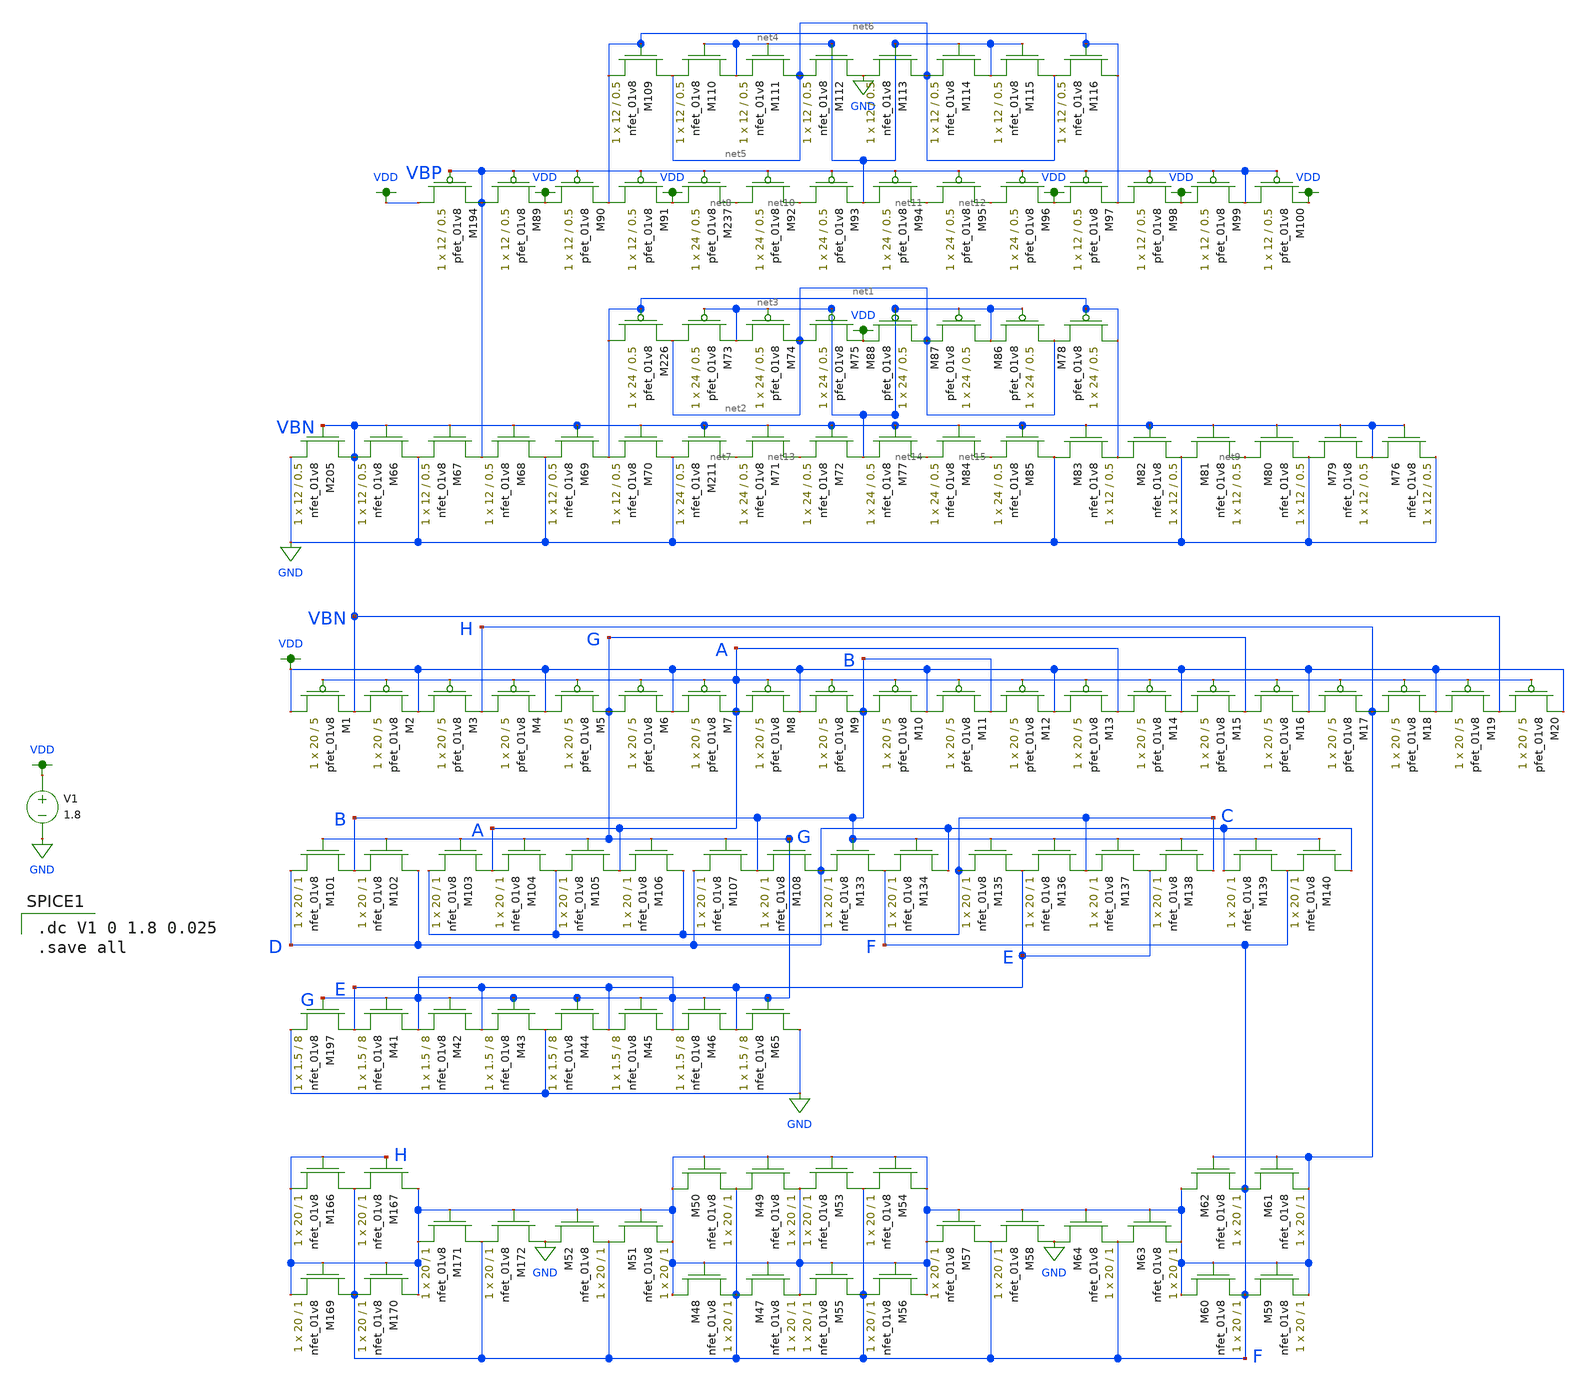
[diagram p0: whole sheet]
** sch_path: miniproject_03/xschem/bias_gen_layout_gen4.sch
**.subckt bias_gen_layout_gen4
XM1 VDD A VBN VDD sky130_fd_pr__pfet_01v8 L=5 W=20 nf=1 ad='int((nf+1)/2) * W/nf * 0.29' as='int((nf+2)/2) * W/nf * 0.29'
+ pd='2*int((nf+1)/2) * (W/nf + 0.29)' ps='2*int((nf+2)/2) * (W/nf + 0.29)' nrd='0.29 / W' nrs='0.29 / W'
+ sa=0 sb=0 sd=0 mult=1 m=1
XM2 VBN A VDD VDD sky130_fd_pr__pfet_01v8 L=5 W=20 nf=1 ad='int((nf+1)/2) * W/nf * 0.29' as='int((nf+2)/2) * W/nf * 0.29'
+ pd='2*int((nf+1)/2) * (W/nf + 0.29)' ps='2*int((nf+2)/2) * (W/nf + 0.29)' nrd='0.29 / W' nrs='0.29 / W'
+ sa=0 sb=0 sd=0 mult=1 m=1
XM3 VDD A H VDD sky130_fd_pr__pfet_01v8 L=5 W=20 nf=1 ad='int((nf+1)/2) * W/nf * 0.29' as='int((nf+2)/2) * W/nf * 0.29'
+ pd='2*int((nf+1)/2) * (W/nf + 0.29)' ps='2*int((nf+2)/2) * (W/nf + 0.29)' nrd='0.29 / W' nrs='0.29 / W'
+ sa=0 sb=0 sd=0 mult=1 m=1
XM4 H A VDD VDD sky130_fd_pr__pfet_01v8 L=5 W=20 nf=1 ad='int((nf+1)/2) * W/nf * 0.29' as='int((nf+2)/2) * W/nf * 0.29'
+ pd='2*int((nf+1)/2) * (W/nf + 0.29)' ps='2*int((nf+2)/2) * (W/nf + 0.29)' nrd='0.29 / W' nrs='0.29 / W'
+ sa=0 sb=0 sd=0 mult=1 m=1
XM5 VDD A G VDD sky130_fd_pr__pfet_01v8 L=5 W=20 nf=1 ad='int((nf+1)/2) * W/nf * 0.29' as='int((nf+2)/2) * W/nf * 0.29'
+ pd='2*int((nf+1)/2) * (W/nf + 0.29)' ps='2*int((nf+2)/2) * (W/nf + 0.29)' nrd='0.29 / W' nrs='0.29 / W'
+ sa=0 sb=0 sd=0 mult=1 m=1
XM6 G A VDD VDD sky130_fd_pr__pfet_01v8 L=5 W=20 nf=1 ad='int((nf+1)/2) * W/nf * 0.29' as='int((nf+2)/2) * W/nf * 0.29'
+ pd='2*int((nf+1)/2) * (W/nf + 0.29)' ps='2*int((nf+2)/2) * (W/nf + 0.29)' nrd='0.29 / W' nrs='0.29 / W'
+ sa=0 sb=0 sd=0 mult=1 m=1
XM7 VDD A A VDD sky130_fd_pr__pfet_01v8 L=5 W=20 nf=1 ad='int((nf+1)/2) * W/nf * 0.29' as='int((nf+2)/2) * W/nf * 0.29'
+ pd='2*int((nf+1)/2) * (W/nf + 0.29)' ps='2*int((nf+2)/2) * (W/nf + 0.29)' nrd='0.29 / W' nrs='0.29 / W'
+ sa=0 sb=0 sd=0 mult=1 m=1
XM8 A A VDD VDD sky130_fd_pr__pfet_01v8 L=5 W=20 nf=1 ad='int((nf+1)/2) * W/nf * 0.29' as='int((nf+2)/2) * W/nf * 0.29'
+ pd='2*int((nf+1)/2) * (W/nf + 0.29)' ps='2*int((nf+2)/2) * (W/nf + 0.29)' nrd='0.29 / W' nrs='0.29 / W'
+ sa=0 sb=0 sd=0 mult=1 m=1
XM9 VDD A B VDD sky130_fd_pr__pfet_01v8 L=5 W=20 nf=1 ad='int((nf+1)/2) * W/nf * 0.29' as='int((nf+2)/2) * W/nf * 0.29'
+ pd='2*int((nf+1)/2) * (W/nf + 0.29)' ps='2*int((nf+2)/2) * (W/nf + 0.29)' nrd='0.29 / W' nrs='0.29 / W'
+ sa=0 sb=0 sd=0 mult=1 m=1
XM10 B A VDD VDD sky130_fd_pr__pfet_01v8 L=5 W=20 nf=1 ad='int((nf+1)/2) * W/nf * 0.29' as='int((nf+2)/2) * W/nf * 0.29'
+ pd='2*int((nf+1)/2) * (W/nf + 0.29)' ps='2*int((nf+2)/2) * (W/nf + 0.29)' nrd='0.29 / W' nrs='0.29 / W'
+ sa=0 sb=0 sd=0 mult=1 m=1
XM11 VDD A B VDD sky130_fd_pr__pfet_01v8 L=5 W=20 nf=1 ad='int((nf+1)/2) * W/nf * 0.29' as='int((nf+2)/2) * W/nf * 0.29'
+ pd='2*int((nf+1)/2) * (W/nf + 0.29)' ps='2*int((nf+2)/2) * (W/nf + 0.29)' nrd='0.29 / W' nrs='0.29 / W'
+ sa=0 sb=0 sd=0 mult=1 m=1
XM12 B A VDD VDD sky130_fd_pr__pfet_01v8 L=5 W=20 nf=1 ad='int((nf+1)/2) * W/nf * 0.29' as='int((nf+2)/2) * W/nf * 0.29'
+ pd='2*int((nf+1)/2) * (W/nf + 0.29)' ps='2*int((nf+2)/2) * (W/nf + 0.29)' nrd='0.29 / W' nrs='0.29 / W'
+ sa=0 sb=0 sd=0 mult=1 m=1
XM13 VDD A A VDD sky130_fd_pr__pfet_01v8 L=5 W=20 nf=1 ad='int((nf+1)/2) * W/nf * 0.29' as='int((nf+2)/2) * W/nf * 0.29'
+ pd='2*int((nf+1)/2) * (W/nf + 0.29)' ps='2*int((nf+2)/2) * (W/nf + 0.29)' nrd='0.29 / W' nrs='0.29 / W'
+ sa=0 sb=0 sd=0 mult=1 m=1
XM14 A A VDD VDD sky130_fd_pr__pfet_01v8 L=5 W=20 nf=1 ad='int((nf+1)/2) * W/nf * 0.29' as='int((nf+2)/2) * W/nf * 0.29'
+ pd='2*int((nf+1)/2) * (W/nf + 0.29)' ps='2*int((nf+2)/2) * (W/nf + 0.29)' nrd='0.29 / W' nrs='0.29 / W'
+ sa=0 sb=0 sd=0 mult=1 m=1
XM15 VDD A G VDD sky130_fd_pr__pfet_01v8 L=5 W=20 nf=1 ad='int((nf+1)/2) * W/nf * 0.29' as='int((nf+2)/2) * W/nf * 0.29'
+ pd='2*int((nf+1)/2) * (W/nf + 0.29)' ps='2*int((nf+2)/2) * (W/nf + 0.29)' nrd='0.29 / W' nrs='0.29 / W'
+ sa=0 sb=0 sd=0 mult=1 m=1
XM16 G A VDD VDD sky130_fd_pr__pfet_01v8 L=5 W=20 nf=1 ad='int((nf+1)/2) * W/nf * 0.29' as='int((nf+2)/2) * W/nf * 0.29'
+ pd='2*int((nf+1)/2) * (W/nf + 0.29)' ps='2*int((nf+2)/2) * (W/nf + 0.29)' nrd='0.29 / W' nrs='0.29 / W'
+ sa=0 sb=0 sd=0 mult=1 m=1
XM17 VDD A H VDD sky130_fd_pr__pfet_01v8 L=5 W=20 nf=1 ad='int((nf+1)/2) * W/nf * 0.29' as='int((nf+2)/2) * W/nf * 0.29'
+ pd='2*int((nf+1)/2) * (W/nf + 0.29)' ps='2*int((nf+2)/2) * (W/nf + 0.29)' nrd='0.29 / W' nrs='0.29 / W'
+ sa=0 sb=0 sd=0 mult=1 m=1
XM18 H A VDD VDD sky130_fd_pr__pfet_01v8 L=5 W=20 nf=1 ad='int((nf+1)/2) * W/nf * 0.29' as='int((nf+2)/2) * W/nf * 0.29'
+ pd='2*int((nf+1)/2) * (W/nf + 0.29)' ps='2*int((nf+2)/2) * (W/nf + 0.29)' nrd='0.29 / W' nrs='0.29 / W'
+ sa=0 sb=0 sd=0 mult=1 m=1
XM19 VDD A VBN VDD sky130_fd_pr__pfet_01v8 L=5 W=20 nf=1 ad='int((nf+1)/2) * W/nf * 0.29' as='int((nf+2)/2) * W/nf * 0.29'
+ pd='2*int((nf+1)/2) * (W/nf + 0.29)' ps='2*int((nf+2)/2) * (W/nf + 0.29)' nrd='0.29 / W' nrs='0.29 / W'
+ sa=0 sb=0 sd=0 mult=1 m=1
XM20 VBN A VDD VDD sky130_fd_pr__pfet_01v8 L=5 W=20 nf=1 ad='int((nf+1)/2) * W/nf * 0.29' as='int((nf+2)/2) * W/nf * 0.29'
+ pd='2*int((nf+1)/2) * (W/nf + 0.29)' ps='2*int((nf+2)/2) * (W/nf + 0.29)' nrd='0.29 / W' nrs='0.29 / W'
+ sa=0 sb=0 sd=0 mult=1 m=1
XM166 F H H GND sky130_fd_pr__nfet_01v8 L=1 W=20 nf=1 ad='int((nf+1)/2) * W/nf * 0.29' as='int((nf+2)/2) * W/nf * 0.29'
+ pd='2*int((nf+1)/2) * (W/nf + 0.29)' ps='2*int((nf+2)/2) * (W/nf + 0.29)' nrd='0.29 / W' nrs='0.29 / W'
+ sa=0 sb=0 sd=0 mult=1 m=1
XM167 H H F GND sky130_fd_pr__nfet_01v8 L=1 W=20 nf=1 ad='int((nf+1)/2) * W/nf * 0.29' as='int((nf+2)/2) * W/nf * 0.29'
+ pd='2*int((nf+1)/2) * (W/nf + 0.29)' ps='2*int((nf+2)/2) * (W/nf + 0.29)' nrd='0.29 / W' nrs='0.29 / W'
+ sa=0 sb=0 sd=0 mult=1 m=1
XM169 F H H GND sky130_fd_pr__nfet_01v8 L=1 W=20 nf=1 ad='int((nf+1)/2) * W/nf * 0.29' as='int((nf+2)/2) * W/nf * 0.29'
+ pd='2*int((nf+1)/2) * (W/nf + 0.29)' ps='2*int((nf+2)/2) * (W/nf + 0.29)' nrd='0.29 / W' nrs='0.29 / W'
+ sa=0 sb=0 sd=0 mult=1 m=1
XM170 H H F GND sky130_fd_pr__nfet_01v8 L=1 W=20 nf=1 ad='int((nf+1)/2) * W/nf * 0.29' as='int((nf+2)/2) * W/nf * 0.29'
+ pd='2*int((nf+1)/2) * (W/nf + 0.29)' ps='2*int((nf+2)/2) * (W/nf + 0.29)' nrd='0.29 / W' nrs='0.29 / W'
+ sa=0 sb=0 sd=0 mult=1 m=1
XM171 F H H GND sky130_fd_pr__nfet_01v8 L=1 W=20 nf=1 ad='int((nf+1)/2) * W/nf * 0.29' as='int((nf+2)/2) * W/nf * 0.29'
+ pd='2*int((nf+1)/2) * (W/nf + 0.29)' ps='2*int((nf+2)/2) * (W/nf + 0.29)' nrd='0.29 / W' nrs='0.29 / W'
+ sa=0 sb=0 sd=0 mult=1 m=1
XM172 GND H F GND sky130_fd_pr__nfet_01v8 L=1 W=20 nf=1 ad='int((nf+1)/2) * W/nf * 0.29' as='int((nf+2)/2) * W/nf * 0.29'
+ pd='2*int((nf+1)/2) * (W/nf + 0.29)' ps='2*int((nf+2)/2) * (W/nf + 0.29)' nrd='0.29 / W' nrs='0.29 / W'
+ sa=0 sb=0 sd=0 mult=1 m=1
XM197 E G GND GND sky130_fd_pr__nfet_01v8 L=8 W=1.5 nf=1 ad='int((nf+1)/2) * W/nf * 0.29' as='int((nf+2)/2) * W/nf * 0.29'
+ pd='2*int((nf+1)/2) * (W/nf + 0.29)' ps='2*int((nf+2)/2) * (W/nf + 0.29)' nrd='0.29 / W' nrs='0.29 / W'
+ sa=0 sb=0 sd=0 mult=1 m=1
XM205 VBN VBN GND GND sky130_fd_pr__nfet_01v8 L=0.5 W=12 nf=1 ad='int((nf+1)/2) * W/nf * 0.29' as='int((nf+2)/2) * W/nf * 0.29'
+ pd='2*int((nf+1)/2) * (W/nf + 0.29)' ps='2*int((nf+2)/2) * (W/nf + 0.29)' nrd='0.29 / W' nrs='0.29 / W'
+ sa=0 sb=0 sd=0 mult=1 m=1
XM211 net7 VBN GND GND sky130_fd_pr__nfet_01v8 L=0.5 W=24 nf=1 ad='int((nf+1)/2) * W/nf * 0.29' as='int((nf+2)/2) * W/nf * 0.29'
+ pd='2*int((nf+1)/2) * (W/nf + 0.29)' ps='2*int((nf+2)/2) * (W/nf + 0.29)' nrd='0.29 / W' nrs='0.29 / W'
+ sa=0 sb=0 sd=0 mult=1 m=1
XM226 net1 net1 net2 VDD sky130_fd_pr__pfet_01v8 L=0.5 W=24 nf=1 ad='int((nf+1)/2) * W/nf * 0.29' as='int((nf+2)/2) * W/nf * 0.29'
+ pd='2*int((nf+1)/2) * (W/nf + 0.29)' ps='2*int((nf+2)/2) * (W/nf + 0.29)' nrd='0.29 / W' nrs='0.29 / W'
+ sa=0 sb=0 sd=0 mult=1 m=1
XM237 VDD VBP net8 VDD sky130_fd_pr__pfet_01v8 L=0.5 W=24 nf=1 ad='int((nf+1)/2) * W/nf * 0.29' as='int((nf+2)/2) * W/nf * 0.29'
+ pd='2*int((nf+1)/2) * (W/nf + 0.29)' ps='2*int((nf+2)/2) * (W/nf + 0.29)' nrd='0.29 / W' nrs='0.29 / W'
+ sa=0 sb=0 sd=0 mult=1 m=1
XM101 B G D GND sky130_fd_pr__nfet_01v8 L=1 W=20 nf=1 ad='int((nf+1)/2) * W/nf * 0.29' as='int((nf+2)/2) * W/nf * 0.29'
+ pd='2*int((nf+1)/2) * (W/nf + 0.29)' ps='2*int((nf+2)/2) * (W/nf + 0.29)' nrd='0.29 / W' nrs='0.29 / W'
+ sa=0 sb=0 sd=0 mult=1 m=1
XM102 D G B GND sky130_fd_pr__nfet_01v8 L=1 W=20 nf=1 ad='int((nf+1)/2) * W/nf * 0.29' as='int((nf+2)/2) * W/nf * 0.29'
+ pd='2*int((nf+1)/2) * (W/nf + 0.29)' ps='2*int((nf+2)/2) * (W/nf + 0.29)' nrd='0.29 / W' nrs='0.29 / W'
+ sa=0 sb=0 sd=0 mult=1 m=1
XM103 A G C GND sky130_fd_pr__nfet_01v8 L=1 W=20 nf=1 ad='int((nf+1)/2) * W/nf * 0.29' as='int((nf+2)/2) * W/nf * 0.29'
+ pd='2*int((nf+1)/2) * (W/nf + 0.29)' ps='2*int((nf+2)/2) * (W/nf + 0.29)' nrd='0.29 / W' nrs='0.29 / W'
+ sa=0 sb=0 sd=0 mult=1 m=1
XM104 C G A GND sky130_fd_pr__nfet_01v8 L=1 W=20 nf=1 ad='int((nf+1)/2) * W/nf * 0.29' as='int((nf+2)/2) * W/nf * 0.29'
+ pd='2*int((nf+1)/2) * (W/nf + 0.29)' ps='2*int((nf+2)/2) * (W/nf + 0.29)' nrd='0.29 / W' nrs='0.29 / W'
+ sa=0 sb=0 sd=0 mult=1 m=1
XM105 A G C GND sky130_fd_pr__nfet_01v8 L=1 W=20 nf=1 ad='int((nf+1)/2) * W/nf * 0.29' as='int((nf+2)/2) * W/nf * 0.29'
+ pd='2*int((nf+1)/2) * (W/nf + 0.29)' ps='2*int((nf+2)/2) * (W/nf + 0.29)' nrd='0.29 / W' nrs='0.29 / W'
+ sa=0 sb=0 sd=0 mult=1 m=1
XM106 C G A GND sky130_fd_pr__nfet_01v8 L=1 W=20 nf=1 ad='int((nf+1)/2) * W/nf * 0.29' as='int((nf+2)/2) * W/nf * 0.29'
+ pd='2*int((nf+1)/2) * (W/nf + 0.29)' ps='2*int((nf+2)/2) * (W/nf + 0.29)' nrd='0.29 / W' nrs='0.29 / W'
+ sa=0 sb=0 sd=0 mult=1 m=1
XM107 B G D GND sky130_fd_pr__nfet_01v8 L=1 W=20 nf=1 ad='int((nf+1)/2) * W/nf * 0.29' as='int((nf+2)/2) * W/nf * 0.29'
+ pd='2*int((nf+1)/2) * (W/nf + 0.29)' ps='2*int((nf+2)/2) * (W/nf + 0.29)' nrd='0.29 / W' nrs='0.29 / W'
+ sa=0 sb=0 sd=0 mult=1 m=1
XM108 D G B GND sky130_fd_pr__nfet_01v8 L=1 W=20 nf=1 ad='int((nf+1)/2) * W/nf * 0.29' as='int((nf+2)/2) * W/nf * 0.29'
+ pd='2*int((nf+1)/2) * (W/nf + 0.29)' ps='2*int((nf+2)/2) * (W/nf + 0.29)' nrd='0.29 / W' nrs='0.29 / W'
+ sa=0 sb=0 sd=0 mult=1 m=1
XM133 F B D GND sky130_fd_pr__nfet_01v8 L=1 W=20 nf=1 ad='int((nf+1)/2) * W/nf * 0.29' as='int((nf+2)/2) * W/nf * 0.29'
+ pd='2*int((nf+1)/2) * (W/nf + 0.29)' ps='2*int((nf+2)/2) * (W/nf + 0.29)' nrd='0.29 / W' nrs='0.29 / W'
+ sa=0 sb=0 sd=0 mult=1 m=1
XM134 D B F GND sky130_fd_pr__nfet_01v8 L=1 W=20 nf=1 ad='int((nf+1)/2) * W/nf * 0.29' as='int((nf+2)/2) * W/nf * 0.29'
+ pd='2*int((nf+1)/2) * (W/nf + 0.29)' ps='2*int((nf+2)/2) * (W/nf + 0.29)' nrd='0.29 / W' nrs='0.29 / W'
+ sa=0 sb=0 sd=0 mult=1 m=1
XM135 E B C GND sky130_fd_pr__nfet_01v8 L=1 W=20 nf=1 ad='int((nf+1)/2) * W/nf * 0.29' as='int((nf+2)/2) * W/nf * 0.29'
+ pd='2*int((nf+1)/2) * (W/nf + 0.29)' ps='2*int((nf+2)/2) * (W/nf + 0.29)' nrd='0.29 / W' nrs='0.29 / W'
+ sa=0 sb=0 sd=0 mult=1 m=1
XM136 C B E GND sky130_fd_pr__nfet_01v8 L=1 W=20 nf=1 ad='int((nf+1)/2) * W/nf * 0.29' as='int((nf+2)/2) * W/nf * 0.29'
+ pd='2*int((nf+1)/2) * (W/nf + 0.29)' ps='2*int((nf+2)/2) * (W/nf + 0.29)' nrd='0.29 / W' nrs='0.29 / W'
+ sa=0 sb=0 sd=0 mult=1 m=1
XM137 E B C GND sky130_fd_pr__nfet_01v8 L=1 W=20 nf=1 ad='int((nf+1)/2) * W/nf * 0.29' as='int((nf+2)/2) * W/nf * 0.29'
+ pd='2*int((nf+1)/2) * (W/nf + 0.29)' ps='2*int((nf+2)/2) * (W/nf + 0.29)' nrd='0.29 / W' nrs='0.29 / W'
+ sa=0 sb=0 sd=0 mult=1 m=1
XM138 C B E GND sky130_fd_pr__nfet_01v8 L=1 W=20 nf=1 ad='int((nf+1)/2) * W/nf * 0.29' as='int((nf+2)/2) * W/nf * 0.29'
+ pd='2*int((nf+1)/2) * (W/nf + 0.29)' ps='2*int((nf+2)/2) * (W/nf + 0.29)' nrd='0.29 / W' nrs='0.29 / W'
+ sa=0 sb=0 sd=0 mult=1 m=1
XM139 F B D GND sky130_fd_pr__nfet_01v8 L=1 W=20 nf=1 ad='int((nf+1)/2) * W/nf * 0.29' as='int((nf+2)/2) * W/nf * 0.29'
+ pd='2*int((nf+1)/2) * (W/nf + 0.29)' ps='2*int((nf+2)/2) * (W/nf + 0.29)' nrd='0.29 / W' nrs='0.29 / W'
+ sa=0 sb=0 sd=0 mult=1 m=1
XM140 D B F GND sky130_fd_pr__nfet_01v8 L=1 W=20 nf=1 ad='int((nf+1)/2) * W/nf * 0.29' as='int((nf+2)/2) * W/nf * 0.29'
+ pd='2*int((nf+1)/2) * (W/nf + 0.29)' ps='2*int((nf+2)/2) * (W/nf + 0.29)' nrd='0.29 / W' nrs='0.29 / W'
+ sa=0 sb=0 sd=0 mult=1 m=1
XM194 VDD VBP VBP VDD sky130_fd_pr__pfet_01v8 L=0.5 W=12 nf=1 ad='int((nf+1)/2) * W/nf * 0.29' as='int((nf+2)/2) * W/nf * 0.29'
+ pd='2*int((nf+1)/2) * (W/nf + 0.29)' ps='2*int((nf+2)/2) * (W/nf + 0.29)' nrd='0.29 / W' nrs='0.29 / W'
+ sa=0 sb=0 sd=0 mult=1 m=1
V1 VDD GND 1.8
XM41 G G E GND sky130_fd_pr__nfet_01v8 L=8 W=1.5 nf=1 ad='int((nf+1)/2) * W/nf * 0.29' as='int((nf+2)/2) * W/nf * 0.29'
+ pd='2*int((nf+1)/2) * (W/nf + 0.29)' ps='2*int((nf+2)/2) * (W/nf + 0.29)' nrd='0.29 / W' nrs='0.29 / W'
+ sa=0 sb=0 sd=0 mult=1 m=1
XM42 E G G GND sky130_fd_pr__nfet_01v8 L=8 W=1.5 nf=1 ad='int((nf+1)/2) * W/nf * 0.29' as='int((nf+2)/2) * W/nf * 0.29'
+ pd='2*int((nf+1)/2) * (W/nf + 0.29)' ps='2*int((nf+2)/2) * (W/nf + 0.29)' nrd='0.29 / W' nrs='0.29 / W'
+ sa=0 sb=0 sd=0 mult=1 m=1
XM43 GND G E GND sky130_fd_pr__nfet_01v8 L=8 W=1.5 nf=1 ad='int((nf+1)/2) * W/nf * 0.29' as='int((nf+2)/2) * W/nf * 0.29'
+ pd='2*int((nf+1)/2) * (W/nf + 0.29)' ps='2*int((nf+2)/2) * (W/nf + 0.29)' nrd='0.29 / W' nrs='0.29 / W'
+ sa=0 sb=0 sd=0 mult=1 m=1
XM44 E G GND GND sky130_fd_pr__nfet_01v8 L=8 W=1.5 nf=1 ad='int((nf+1)/2) * W/nf * 0.29' as='int((nf+2)/2) * W/nf * 0.29'
+ pd='2*int((nf+1)/2) * (W/nf + 0.29)' ps='2*int((nf+2)/2) * (W/nf + 0.29)' nrd='0.29 / W' nrs='0.29 / W'
+ sa=0 sb=0 sd=0 mult=1 m=1
XM45 G G E GND sky130_fd_pr__nfet_01v8 L=8 W=1.5 nf=1 ad='int((nf+1)/2) * W/nf * 0.29' as='int((nf+2)/2) * W/nf * 0.29'
+ pd='2*int((nf+1)/2) * (W/nf + 0.29)' ps='2*int((nf+2)/2) * (W/nf + 0.29)' nrd='0.29 / W' nrs='0.29 / W'
+ sa=0 sb=0 sd=0 mult=1 m=1
XM46 E G G GND sky130_fd_pr__nfet_01v8 L=8 W=1.5 nf=1 ad='int((nf+1)/2) * W/nf * 0.29' as='int((nf+2)/2) * W/nf * 0.29'
+ pd='2*int((nf+1)/2) * (W/nf + 0.29)' ps='2*int((nf+2)/2) * (W/nf + 0.29)' nrd='0.29 / W' nrs='0.29 / W'
+ sa=0 sb=0 sd=0 mult=1 m=1
XM47 F H H GND sky130_fd_pr__nfet_01v8 L=1 W=20 nf=1 ad='int((nf+1)/2) * W/nf * 0.29' as='int((nf+2)/2) * W/nf * 0.29'
+ pd='2*int((nf+1)/2) * (W/nf + 0.29)' ps='2*int((nf+2)/2) * (W/nf + 0.29)' nrd='0.29 / W' nrs='0.29 / W'
+ sa=0 sb=0 sd=0 mult=1 m=1
XM48 H H F GND sky130_fd_pr__nfet_01v8 L=1 W=20 nf=1 ad='int((nf+1)/2) * W/nf * 0.29' as='int((nf+2)/2) * W/nf * 0.29'
+ pd='2*int((nf+1)/2) * (W/nf + 0.29)' ps='2*int((nf+2)/2) * (W/nf + 0.29)' nrd='0.29 / W' nrs='0.29 / W'
+ sa=0 sb=0 sd=0 mult=1 m=1
XM49 F H H GND sky130_fd_pr__nfet_01v8 L=1 W=20 nf=1 ad='int((nf+1)/2) * W/nf * 0.29' as='int((nf+2)/2) * W/nf * 0.29'
+ pd='2*int((nf+1)/2) * (W/nf + 0.29)' ps='2*int((nf+2)/2) * (W/nf + 0.29)' nrd='0.29 / W' nrs='0.29 / W'
+ sa=0 sb=0 sd=0 mult=1 m=1
XM50 H H F GND sky130_fd_pr__nfet_01v8 L=1 W=20 nf=1 ad='int((nf+1)/2) * W/nf * 0.29' as='int((nf+2)/2) * W/nf * 0.29'
+ pd='2*int((nf+1)/2) * (W/nf + 0.29)' ps='2*int((nf+2)/2) * (W/nf + 0.29)' nrd='0.29 / W' nrs='0.29 / W'
+ sa=0 sb=0 sd=0 mult=1 m=1
XM51 F H H GND sky130_fd_pr__nfet_01v8 L=1 W=20 nf=1 ad='int((nf+1)/2) * W/nf * 0.29' as='int((nf+2)/2) * W/nf * 0.29'
+ pd='2*int((nf+1)/2) * (W/nf + 0.29)' ps='2*int((nf+2)/2) * (W/nf + 0.29)' nrd='0.29 / W' nrs='0.29 / W'
+ sa=0 sb=0 sd=0 mult=1 m=1
XM52 GND H F GND sky130_fd_pr__nfet_01v8 L=1 W=20 nf=1 ad='int((nf+1)/2) * W/nf * 0.29' as='int((nf+2)/2) * W/nf * 0.29'
+ pd='2*int((nf+1)/2) * (W/nf + 0.29)' ps='2*int((nf+2)/2) * (W/nf + 0.29)' nrd='0.29 / W' nrs='0.29 / W'
+ sa=0 sb=0 sd=0 mult=1 m=1
XM53 F H H GND sky130_fd_pr__nfet_01v8 L=1 W=20 nf=1 ad='int((nf+1)/2) * W/nf * 0.29' as='int((nf+2)/2) * W/nf * 0.29'
+ pd='2*int((nf+1)/2) * (W/nf + 0.29)' ps='2*int((nf+2)/2) * (W/nf + 0.29)' nrd='0.29 / W' nrs='0.29 / W'
+ sa=0 sb=0 sd=0 mult=1 m=1
XM54 H H F GND sky130_fd_pr__nfet_01v8 L=1 W=20 nf=1 ad='int((nf+1)/2) * W/nf * 0.29' as='int((nf+2)/2) * W/nf * 0.29'
+ pd='2*int((nf+1)/2) * (W/nf + 0.29)' ps='2*int((nf+2)/2) * (W/nf + 0.29)' nrd='0.29 / W' nrs='0.29 / W'
+ sa=0 sb=0 sd=0 mult=1 m=1
XM55 F H H GND sky130_fd_pr__nfet_01v8 L=1 W=20 nf=1 ad='int((nf+1)/2) * W/nf * 0.29' as='int((nf+2)/2) * W/nf * 0.29'
+ pd='2*int((nf+1)/2) * (W/nf + 0.29)' ps='2*int((nf+2)/2) * (W/nf + 0.29)' nrd='0.29 / W' nrs='0.29 / W'
+ sa=0 sb=0 sd=0 mult=1 m=1
XM56 H H F GND sky130_fd_pr__nfet_01v8 L=1 W=20 nf=1 ad='int((nf+1)/2) * W/nf * 0.29' as='int((nf+2)/2) * W/nf * 0.29'
+ pd='2*int((nf+1)/2) * (W/nf + 0.29)' ps='2*int((nf+2)/2) * (W/nf + 0.29)' nrd='0.29 / W' nrs='0.29 / W'
+ sa=0 sb=0 sd=0 mult=1 m=1
XM57 F H H GND sky130_fd_pr__nfet_01v8 L=1 W=20 nf=1 ad='int((nf+1)/2) * W/nf * 0.29' as='int((nf+2)/2) * W/nf * 0.29'
+ pd='2*int((nf+1)/2) * (W/nf + 0.29)' ps='2*int((nf+2)/2) * (W/nf + 0.29)' nrd='0.29 / W' nrs='0.29 / W'
+ sa=0 sb=0 sd=0 mult=1 m=1
XM58 GND H F GND sky130_fd_pr__nfet_01v8 L=1 W=20 nf=1 ad='int((nf+1)/2) * W/nf * 0.29' as='int((nf+2)/2) * W/nf * 0.29'
+ pd='2*int((nf+1)/2) * (W/nf + 0.29)' ps='2*int((nf+2)/2) * (W/nf + 0.29)' nrd='0.29 / W' nrs='0.29 / W'
+ sa=0 sb=0 sd=0 mult=1 m=1
XM59 F H H GND sky130_fd_pr__nfet_01v8 L=1 W=20 nf=1 ad='int((nf+1)/2) * W/nf * 0.29' as='int((nf+2)/2) * W/nf * 0.29'
+ pd='2*int((nf+1)/2) * (W/nf + 0.29)' ps='2*int((nf+2)/2) * (W/nf + 0.29)' nrd='0.29 / W' nrs='0.29 / W'
+ sa=0 sb=0 sd=0 mult=1 m=1
XM60 H H F GND sky130_fd_pr__nfet_01v8 L=1 W=20 nf=1 ad='int((nf+1)/2) * W/nf * 0.29' as='int((nf+2)/2) * W/nf * 0.29'
+ pd='2*int((nf+1)/2) * (W/nf + 0.29)' ps='2*int((nf+2)/2) * (W/nf + 0.29)' nrd='0.29 / W' nrs='0.29 / W'
+ sa=0 sb=0 sd=0 mult=1 m=1
XM61 F H H GND sky130_fd_pr__nfet_01v8 L=1 W=20 nf=1 ad='int((nf+1)/2) * W/nf * 0.29' as='int((nf+2)/2) * W/nf * 0.29'
+ pd='2*int((nf+1)/2) * (W/nf + 0.29)' ps='2*int((nf+2)/2) * (W/nf + 0.29)' nrd='0.29 / W' nrs='0.29 / W'
+ sa=0 sb=0 sd=0 mult=1 m=1
XM62 H H F GND sky130_fd_pr__nfet_01v8 L=1 W=20 nf=1 ad='int((nf+1)/2) * W/nf * 0.29' as='int((nf+2)/2) * W/nf * 0.29'
+ pd='2*int((nf+1)/2) * (W/nf + 0.29)' ps='2*int((nf+2)/2) * (W/nf + 0.29)' nrd='0.29 / W' nrs='0.29 / W'
+ sa=0 sb=0 sd=0 mult=1 m=1
XM63 F H H GND sky130_fd_pr__nfet_01v8 L=1 W=20 nf=1 ad='int((nf+1)/2) * W/nf * 0.29' as='int((nf+2)/2) * W/nf * 0.29'
+ pd='2*int((nf+1)/2) * (W/nf + 0.29)' ps='2*int((nf+2)/2) * (W/nf + 0.29)' nrd='0.29 / W' nrs='0.29 / W'
+ sa=0 sb=0 sd=0 mult=1 m=1
XM64 GND H F GND sky130_fd_pr__nfet_01v8 L=1 W=20 nf=1 ad='int((nf+1)/2) * W/nf * 0.29' as='int((nf+2)/2) * W/nf * 0.29'
+ pd='2*int((nf+1)/2) * (W/nf + 0.29)' ps='2*int((nf+2)/2) * (W/nf + 0.29)' nrd='0.29 / W' nrs='0.29 / W'
+ sa=0 sb=0 sd=0 mult=1 m=1
XM65 GND G E GND sky130_fd_pr__nfet_01v8 L=8 W=1.5 nf=1 ad='int((nf+1)/2) * W/nf * 0.29' as='int((nf+2)/2) * W/nf * 0.29'
+ pd='2*int((nf+1)/2) * (W/nf + 0.29)' ps='2*int((nf+2)/2) * (W/nf + 0.29)' nrd='0.29 / W' nrs='0.29 / W'
+ sa=0 sb=0 sd=0 mult=1 m=1
XM66 GND VBN VBN GND sky130_fd_pr__nfet_01v8 L=0.5 W=12 nf=1 ad='int((nf+1)/2) * W/nf * 0.29' as='int((nf+2)/2) * W/nf * 0.29'
+ pd='2*int((nf+1)/2) * (W/nf + 0.29)' ps='2*int((nf+2)/2) * (W/nf + 0.29)' nrd='0.29 / W' nrs='0.29 / W'
+ sa=0 sb=0 sd=0 mult=1 m=1
XM67 VBP VBN GND GND sky130_fd_pr__nfet_01v8 L=0.5 W=12 nf=1 ad='int((nf+1)/2) * W/nf * 0.29' as='int((nf+2)/2) * W/nf * 0.29'
+ pd='2*int((nf+1)/2) * (W/nf + 0.29)' ps='2*int((nf+2)/2) * (W/nf + 0.29)' nrd='0.29 / W' nrs='0.29 / W'
+ sa=0 sb=0 sd=0 mult=1 m=1
XM68 GND VBN VBP GND sky130_fd_pr__nfet_01v8 L=0.5 W=12 nf=1 ad='int((nf+1)/2) * W/nf * 0.29' as='int((nf+2)/2) * W/nf * 0.29'
+ pd='2*int((nf+1)/2) * (W/nf + 0.29)' ps='2*int((nf+2)/2) * (W/nf + 0.29)' nrd='0.29 / W' nrs='0.29 / W'
+ sa=0 sb=0 sd=0 mult=1 m=1
XM69 net1 VBN GND GND sky130_fd_pr__nfet_01v8 L=0.5 W=12 nf=1 ad='int((nf+1)/2) * W/nf * 0.29' as='int((nf+2)/2) * W/nf * 0.29'
+ pd='2*int((nf+1)/2) * (W/nf + 0.29)' ps='2*int((nf+2)/2) * (W/nf + 0.29)' nrd='0.29 / W' nrs='0.29 / W'
+ sa=0 sb=0 sd=0 mult=1 m=1
XM70 GND VBN net1 GND sky130_fd_pr__nfet_01v8 L=0.5 W=12 nf=1 ad='int((nf+1)/2) * W/nf * 0.29' as='int((nf+2)/2) * W/nf * 0.29'
+ pd='2*int((nf+1)/2) * (W/nf + 0.29)' ps='2*int((nf+2)/2) * (W/nf + 0.29)' nrd='0.29 / W' nrs='0.29 / W'
+ sa=0 sb=0 sd=0 mult=1 m=1
XM73 net2 net3 net3 VDD sky130_fd_pr__pfet_01v8 L=0.5 W=24 nf=1 ad='int((nf+1)/2) * W/nf * 0.29' as='int((nf+2)/2) * W/nf * 0.29'
+ pd='2*int((nf+1)/2) * (W/nf + 0.29)' ps='2*int((nf+2)/2) * (W/nf + 0.29)' nrd='0.29 / W' nrs='0.29 / W'
+ sa=0 sb=0 sd=0 mult=1 m=1
XM74 net3 net3 net2 VDD sky130_fd_pr__pfet_01v8 L=0.5 W=24 nf=1 ad='int((nf+1)/2) * W/nf * 0.29' as='int((nf+2)/2) * W/nf * 0.29'
+ pd='2*int((nf+1)/2) * (W/nf + 0.29)' ps='2*int((nf+2)/2) * (W/nf + 0.29)' nrd='0.29 / W' nrs='0.29 / W'
+ sa=0 sb=0 sd=0 mult=1 m=1
XM75 net2 net3 VDD VDD sky130_fd_pr__pfet_01v8 L=0.5 W=24 nf=1 ad='int((nf+1)/2) * W/nf * 0.29' as='int((nf+2)/2) * W/nf * 0.29'
+ pd='2*int((nf+1)/2) * (W/nf + 0.29)' ps='2*int((nf+2)/2) * (W/nf + 0.29)' nrd='0.29 / W' nrs='0.29 / W'
+ sa=0 sb=0 sd=0 mult=1 m=1
XM76 VBN VBN GND GND sky130_fd_pr__nfet_01v8 L=0.5 W=12 nf=1 ad='int((nf+1)/2) * W/nf * 0.29' as='int((nf+2)/2) * W/nf * 0.29'
+ pd='2*int((nf+1)/2) * (W/nf + 0.29)' ps='2*int((nf+2)/2) * (W/nf + 0.29)' nrd='0.29 / W' nrs='0.29 / W'
+ sa=0 sb=0 sd=0 mult=1 m=1
XM78 net1 net1 net2 VDD sky130_fd_pr__pfet_01v8 L=0.5 W=24 nf=1 ad='int((nf+1)/2) * W/nf * 0.29' as='int((nf+2)/2) * W/nf * 0.29'
+ pd='2*int((nf+1)/2) * (W/nf + 0.29)' ps='2*int((nf+2)/2) * (W/nf + 0.29)' nrd='0.29 / W' nrs='0.29 / W'
+ sa=0 sb=0 sd=0 mult=1 m=1
XM79 GND VBN VBN GND sky130_fd_pr__nfet_01v8 L=0.5 W=12 nf=1 ad='int((nf+1)/2) * W/nf * 0.29' as='int((nf+2)/2) * W/nf * 0.29'
+ pd='2*int((nf+1)/2) * (W/nf + 0.29)' ps='2*int((nf+2)/2) * (W/nf + 0.29)' nrd='0.29 / W' nrs='0.29 / W'
+ sa=0 sb=0 sd=0 mult=1 m=1
XM80 net9 VBN GND GND sky130_fd_pr__nfet_01v8 L=0.5 W=12 nf=1 ad='int((nf+1)/2) * W/nf * 0.29' as='int((nf+2)/2) * W/nf * 0.29'
+ pd='2*int((nf+1)/2) * (W/nf + 0.29)' ps='2*int((nf+2)/2) * (W/nf + 0.29)' nrd='0.29 / W' nrs='0.29 / W'
+ sa=0 sb=0 sd=0 mult=1 m=1
XM81 GND VBN net9 GND sky130_fd_pr__nfet_01v8 L=0.5 W=12 nf=1 ad='int((nf+1)/2) * W/nf * 0.29' as='int((nf+2)/2) * W/nf * 0.29'
+ pd='2*int((nf+1)/2) * (W/nf + 0.29)' ps='2*int((nf+2)/2) * (W/nf + 0.29)' nrd='0.29 / W' nrs='0.29 / W'
+ sa=0 sb=0 sd=0 mult=1 m=1
XM82 net1 VBN GND GND sky130_fd_pr__nfet_01v8 L=0.5 W=12 nf=1 ad='int((nf+1)/2) * W/nf * 0.29' as='int((nf+2)/2) * W/nf * 0.29'
+ pd='2*int((nf+1)/2) * (W/nf + 0.29)' ps='2*int((nf+2)/2) * (W/nf + 0.29)' nrd='0.29 / W' nrs='0.29 / W'
+ sa=0 sb=0 sd=0 mult=1 m=1
XM83 GND VBN net1 GND sky130_fd_pr__nfet_01v8 L=0.5 W=12 nf=1 ad='int((nf+1)/2) * W/nf * 0.29' as='int((nf+2)/2) * W/nf * 0.29'
+ pd='2*int((nf+1)/2) * (W/nf + 0.29)' ps='2*int((nf+2)/2) * (W/nf + 0.29)' nrd='0.29 / W' nrs='0.29 / W'
+ sa=0 sb=0 sd=0 mult=1 m=1
XM86 net2 net3 net3 VDD sky130_fd_pr__pfet_01v8 L=0.5 W=24 nf=1 ad='int((nf+1)/2) * W/nf * 0.29' as='int((nf+2)/2) * W/nf * 0.29'
+ pd='2*int((nf+1)/2) * (W/nf + 0.29)' ps='2*int((nf+2)/2) * (W/nf + 0.29)' nrd='0.29 / W' nrs='0.29 / W'
+ sa=0 sb=0 sd=0 mult=1 m=1
XM87 net3 net3 net2 VDD sky130_fd_pr__pfet_01v8 L=0.5 W=24 nf=1 ad='int((nf+1)/2) * W/nf * 0.29' as='int((nf+2)/2) * W/nf * 0.29'
+ pd='2*int((nf+1)/2) * (W/nf + 0.29)' ps='2*int((nf+2)/2) * (W/nf + 0.29)' nrd='0.29 / W' nrs='0.29 / W'
+ sa=0 sb=0 sd=0 mult=1 m=1
XM88 net2 net3 VDD VDD sky130_fd_pr__pfet_01v8 L=0.5 W=24 nf=1 ad='int((nf+1)/2) * W/nf * 0.29' as='int((nf+2)/2) * W/nf * 0.29'
+ pd='2*int((nf+1)/2) * (W/nf + 0.29)' ps='2*int((nf+2)/2) * (W/nf + 0.29)' nrd='0.29 / W' nrs='0.29 / W'
+ sa=0 sb=0 sd=0 mult=1 m=1
XM89 VBP VBP VDD VDD sky130_fd_pr__pfet_01v8 L=0.5 W=12 nf=1 ad='int((nf+1)/2) * W/nf * 0.29' as='int((nf+2)/2) * W/nf * 0.29'
+ pd='2*int((nf+1)/2) * (W/nf + 0.29)' ps='2*int((nf+2)/2) * (W/nf + 0.29)' nrd='0.29 / W' nrs='0.29 / W'
+ sa=0 sb=0 sd=0 mult=1 m=1
XM90 VDD VBP net6 VDD sky130_fd_pr__pfet_01v8 L=0.5 W=12 nf=1 ad='int((nf+1)/2) * W/nf * 0.29' as='int((nf+2)/2) * W/nf * 0.29'
+ pd='2*int((nf+1)/2) * (W/nf + 0.29)' ps='2*int((nf+2)/2) * (W/nf + 0.29)' nrd='0.29 / W' nrs='0.29 / W'
+ sa=0 sb=0 sd=0 mult=1 m=1
XM91 net6 VBP VDD VDD sky130_fd_pr__pfet_01v8 L=0.5 W=12 nf=1 ad='int((nf+1)/2) * W/nf * 0.29' as='int((nf+2)/2) * W/nf * 0.29'
+ pd='2*int((nf+1)/2) * (W/nf + 0.29)' ps='2*int((nf+2)/2) * (W/nf + 0.29)' nrd='0.29 / W' nrs='0.29 / W'
+ sa=0 sb=0 sd=0 mult=1 m=1
XM92 net8 VBP net10 VDD sky130_fd_pr__pfet_01v8 L=0.5 W=24 nf=1 ad='int((nf+1)/2) * W/nf * 0.29' as='int((nf+2)/2) * W/nf * 0.29'
+ pd='2*int((nf+1)/2) * (W/nf + 0.29)' ps='2*int((nf+2)/2) * (W/nf + 0.29)' nrd='0.29 / W' nrs='0.29 / W'
+ sa=0 sb=0 sd=0 mult=1 m=1
XM93 net10 VBP net4 VDD sky130_fd_pr__pfet_01v8 L=0.5 W=24 nf=1 ad='int((nf+1)/2) * W/nf * 0.29' as='int((nf+2)/2) * W/nf * 0.29'
+ pd='2*int((nf+1)/2) * (W/nf + 0.29)' ps='2*int((nf+2)/2) * (W/nf + 0.29)' nrd='0.29 / W' nrs='0.29 / W'
+ sa=0 sb=0 sd=0 mult=1 m=1
XM94 net4 VBP net11 VDD sky130_fd_pr__pfet_01v8 L=0.5 W=24 nf=1 ad='int((nf+1)/2) * W/nf * 0.29' as='int((nf+2)/2) * W/nf * 0.29'
+ pd='2*int((nf+1)/2) * (W/nf + 0.29)' ps='2*int((nf+2)/2) * (W/nf + 0.29)' nrd='0.29 / W' nrs='0.29 / W'
+ sa=0 sb=0 sd=0 mult=1 m=1
XM95 net11 VBP net12 VDD sky130_fd_pr__pfet_01v8 L=0.5 W=24 nf=1 ad='int((nf+1)/2) * W/nf * 0.29' as='int((nf+2)/2) * W/nf * 0.29'
+ pd='2*int((nf+1)/2) * (W/nf + 0.29)' ps='2*int((nf+2)/2) * (W/nf + 0.29)' nrd='0.29 / W' nrs='0.29 / W'
+ sa=0 sb=0 sd=0 mult=1 m=1
XM96 net12 VBP VDD VDD sky130_fd_pr__pfet_01v8 L=0.5 W=24 nf=1 ad='int((nf+1)/2) * W/nf * 0.29' as='int((nf+2)/2) * W/nf * 0.29'
+ pd='2*int((nf+1)/2) * (W/nf + 0.29)' ps='2*int((nf+2)/2) * (W/nf + 0.29)' nrd='0.29 / W' nrs='0.29 / W'
+ sa=0 sb=0 sd=0 mult=1 m=1
XM97 VDD VBP net6 VDD sky130_fd_pr__pfet_01v8 L=0.5 W=12 nf=1 ad='int((nf+1)/2) * W/nf * 0.29' as='int((nf+2)/2) * W/nf * 0.29'
+ pd='2*int((nf+1)/2) * (W/nf + 0.29)' ps='2*int((nf+2)/2) * (W/nf + 0.29)' nrd='0.29 / W' nrs='0.29 / W'
+ sa=0 sb=0 sd=0 mult=1 m=1
XM98 net6 VBP VDD VDD sky130_fd_pr__pfet_01v8 L=0.5 W=12 nf=1 ad='int((nf+1)/2) * W/nf * 0.29' as='int((nf+2)/2) * W/nf * 0.29'
+ pd='2*int((nf+1)/2) * (W/nf + 0.29)' ps='2*int((nf+2)/2) * (W/nf + 0.29)' nrd='0.29 / W' nrs='0.29 / W'
+ sa=0 sb=0 sd=0 mult=1 m=1
XM99 VDD VBP VBP VDD sky130_fd_pr__pfet_01v8 L=0.5 W=12 nf=1 ad='int((nf+1)/2) * W/nf * 0.29' as='int((nf+2)/2) * W/nf * 0.29'
+ pd='2*int((nf+1)/2) * (W/nf + 0.29)' ps='2*int((nf+2)/2) * (W/nf + 0.29)' nrd='0.29 / W' nrs='0.29 / W'
+ sa=0 sb=0 sd=0 mult=1 m=1
XM100 VBP VBP VDD VDD sky130_fd_pr__pfet_01v8 L=0.5 W=12 nf=1 ad='int((nf+1)/2) * W/nf * 0.29' as='int((nf+2)/2) * W/nf * 0.29'
+ pd='2*int((nf+1)/2) * (W/nf + 0.29)' ps='2*int((nf+2)/2) * (W/nf + 0.29)' nrd='0.29 / W' nrs='0.29 / W'
+ sa=0 sb=0 sd=0 mult=1 m=1
XM71 net13 VBN net7 GND sky130_fd_pr__nfet_01v8 L=0.5 W=24 nf=1 ad='int((nf+1)/2) * W/nf * 0.29' as='int((nf+2)/2) * W/nf * 0.29'
+ pd='2*int((nf+1)/2) * (W/nf + 0.29)' ps='2*int((nf+2)/2) * (W/nf + 0.29)' nrd='0.29 / W' nrs='0.29 / W'
+ sa=0 sb=0 sd=0 mult=1 m=1
XM72 net3 VBN net13 GND sky130_fd_pr__nfet_01v8 L=0.5 W=24 nf=1 ad='int((nf+1)/2) * W/nf * 0.29' as='int((nf+2)/2) * W/nf * 0.29'
+ pd='2*int((nf+1)/2) * (W/nf + 0.29)' ps='2*int((nf+2)/2) * (W/nf + 0.29)' nrd='0.29 / W' nrs='0.29 / W'
+ sa=0 sb=0 sd=0 mult=1 m=1
XM77 net14 VBN net3 GND sky130_fd_pr__nfet_01v8 L=0.5 W=24 nf=1 ad='int((nf+1)/2) * W/nf * 0.29' as='int((nf+2)/2) * W/nf * 0.29'
+ pd='2*int((nf+1)/2) * (W/nf + 0.29)' ps='2*int((nf+2)/2) * (W/nf + 0.29)' nrd='0.29 / W' nrs='0.29 / W'
+ sa=0 sb=0 sd=0 mult=1 m=1
XM84 net15 VBN net14 GND sky130_fd_pr__nfet_01v8 L=0.5 W=24 nf=1 ad='int((nf+1)/2) * W/nf * 0.29' as='int((nf+2)/2) * W/nf * 0.29'
+ pd='2*int((nf+1)/2) * (W/nf + 0.29)' ps='2*int((nf+2)/2) * (W/nf + 0.29)' nrd='0.29 / W' nrs='0.29 / W'
+ sa=0 sb=0 sd=0 mult=1 m=1
XM85 GND VBN net15 GND sky130_fd_pr__nfet_01v8 L=0.5 W=24 nf=1 ad='int((nf+1)/2) * W/nf * 0.29' as='int((nf+2)/2) * W/nf * 0.29'
+ pd='2*int((nf+1)/2) * (W/nf + 0.29)' ps='2*int((nf+2)/2) * (W/nf + 0.29)' nrd='0.29 / W' nrs='0.29 / W'
+ sa=0 sb=0 sd=0 mult=1 m=1
XM109 net5 net6 net6 GND sky130_fd_pr__nfet_01v8 L=0.5 W=12 nf=1 ad='int((nf+1)/2) * W/nf * 0.29' as='int((nf+2)/2) * W/nf * 0.29'
+ pd='2*int((nf+1)/2) * (W/nf + 0.29)' ps='2*int((nf+2)/2) * (W/nf + 0.29)' nrd='0.29 / W' nrs='0.29 / W'
+ sa=0 sb=0 sd=0 mult=1 m=1
XM110 net4 net4 net5 GND sky130_fd_pr__nfet_01v8 L=0.5 W=12 nf=1 ad='int((nf+1)/2) * W/nf * 0.29' as='int((nf+2)/2) * W/nf * 0.29'
+ pd='2*int((nf+1)/2) * (W/nf + 0.29)' ps='2*int((nf+2)/2) * (W/nf + 0.29)' nrd='0.29 / W' nrs='0.29 / W'
+ sa=0 sb=0 sd=0 mult=1 m=1
XM111 net5 net4 net4 GND sky130_fd_pr__nfet_01v8 L=0.5 W=12 nf=1 ad='int((nf+1)/2) * W/nf * 0.29' as='int((nf+2)/2) * W/nf * 0.29'
+ pd='2*int((nf+1)/2) * (W/nf + 0.29)' ps='2*int((nf+2)/2) * (W/nf + 0.29)' nrd='0.29 / W' nrs='0.29 / W'
+ sa=0 sb=0 sd=0 mult=1 m=1
XM112 GND net4 net5 GND sky130_fd_pr__nfet_01v8 L=0.5 W=12 nf=1 ad='int((nf+1)/2) * W/nf * 0.29' as='int((nf+2)/2) * W/nf * 0.29'
+ pd='2*int((nf+1)/2) * (W/nf + 0.29)' ps='2*int((nf+2)/2) * (W/nf + 0.29)' nrd='0.29 / W' nrs='0.29 / W'
+ sa=0 sb=0 sd=0 mult=1 m=1
XM113 net5 net4 GND GND sky130_fd_pr__nfet_01v8 L=0.5 W=12 nf=1 ad='int((nf+1)/2) * W/nf * 0.29' as='int((nf+2)/2) * W/nf * 0.29'
+ pd='2*int((nf+1)/2) * (W/nf + 0.29)' ps='2*int((nf+2)/2) * (W/nf + 0.29)' nrd='0.29 / W' nrs='0.29 / W'
+ sa=0 sb=0 sd=0 mult=1 m=1
XM114 net4 net4 net5 GND sky130_fd_pr__nfet_01v8 L=0.5 W=12 nf=1 ad='int((nf+1)/2) * W/nf * 0.29' as='int((nf+2)/2) * W/nf * 0.29'
+ pd='2*int((nf+1)/2) * (W/nf + 0.29)' ps='2*int((nf+2)/2) * (W/nf + 0.29)' nrd='0.29 / W' nrs='0.29 / W'
+ sa=0 sb=0 sd=0 mult=1 m=1
XM115 net5 net4 net4 GND sky130_fd_pr__nfet_01v8 L=0.5 W=12 nf=1 ad='int((nf+1)/2) * W/nf * 0.29' as='int((nf+2)/2) * W/nf * 0.29'
+ pd='2*int((nf+1)/2) * (W/nf + 0.29)' ps='2*int((nf+2)/2) * (W/nf + 0.29)' nrd='0.29 / W' nrs='0.29 / W'
+ sa=0 sb=0 sd=0 mult=1 m=1
XM116 net6 net6 net5 GND sky130_fd_pr__nfet_01v8 L=0.5 W=12 nf=1 ad='int((nf+1)/2) * W/nf * 0.29' as='int((nf+2)/2) * W/nf * 0.29'
+ pd='2*int((nf+1)/2) * (W/nf + 0.29)' ps='2*int((nf+2)/2) * (W/nf + 0.29)' nrd='0.29 / W' nrs='0.29 / W'
+ sa=0 sb=0 sd=0 mult=1 m=1
**** begin user architecture code

.dc V1 0 1.8 0.025
.save all


.option wnflag=1
.lib ~/skywater/skywater-pdk/libraries/sky130_fd_pr_ngspice/latest/models/sky130.lib.spice tt

**** end user architecture code
**.ends
.GLOBAL GND
.GLOBAL VDD
.end
